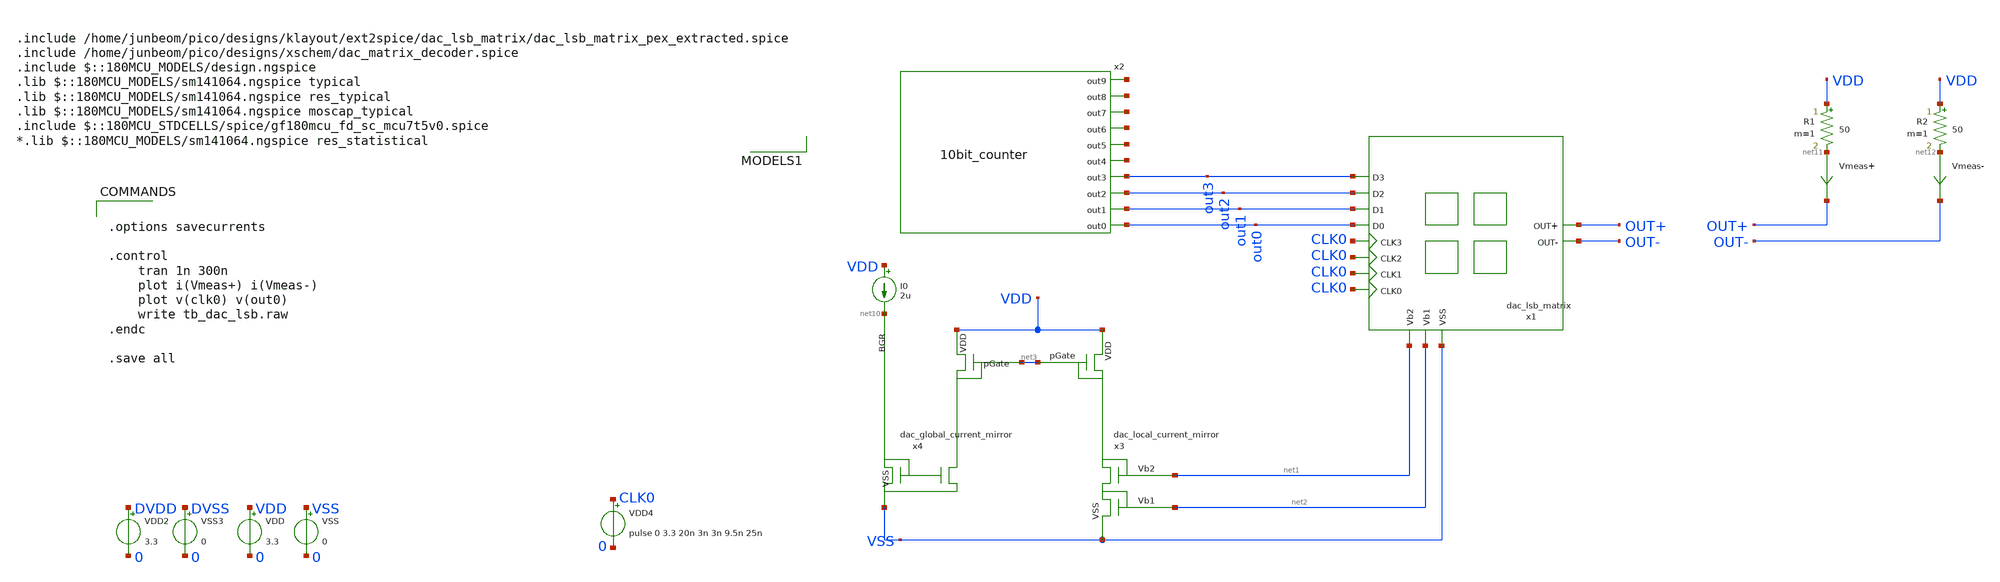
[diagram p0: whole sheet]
** sch_path: DAC/xschem/posim/tb/posim_tb_dac_lsb_matrix.sch
**.subckt posim_tb_dac_lsb_matrix
x2 out0 out1 out2 out3 net4 net5 net6 net7 net8 net9 10bit_counter
VDD VDD 0 3.3
VSS VSS 0 0
VDD2 DVDD 0 3.3
VSS3 DVSS 0 0
x3 VDD net3 net1 net2 VSS dac_local_current_mirror
x4 VDD net3 net10 VSS dac_global_current_mirror
I0 VDD net10 2u
R1 VDD net11 50 m=1
R2 VDD net12 50 m=1
Vmeas+ net11 OUT+ 0
.save i(vmeas+)
Vmeas- net12 OUT- 0
.save i(vmeas-)
x1 out3 out2 out1 out0 CLK0 CLK0 CLK0 CLK0 net1 net2 VSS OUT+ OUT- DVDD VSS dac_lsb_matrix
VDD4 CLK0 0 pulse 0 3.3 20n 3n 3n 9.5n 25n
**** begin user architecture code


.options savecurrents

.control
    tran 1n 300n
    plot i(Vmeas+) i(Vmeas-)
    plot v(clk0) v(out0)
    write tb_dac_lsb.raw
.endc

.save all



.include /home/junbeom/pico/designs/klayout/ext2spice/dac_lsb_matrix/dac_lsb_matrix_pex_extracted.spice
.include /home/junbeom/pico/designs/xschem/dac_matrix_decoder.spice
.include $::180MCU_MODELS/design.ngspice
.lib $::180MCU_MODELS/sm141064.ngspice typical
.lib $::180MCU_MODELS/sm141064.ngspice res_typical
.lib $::180MCU_MODELS/sm141064.ngspice moscap_typical
.include $::180MCU_STDCELLS/spice/gf180mcu_fd_sc_mcu7t5v0.spice
*.lib $::180MCU_MODELS/sm141064.ngspice res_statistical

**** end user architecture code
**.ends

* expanding   symbol:  10bit_counter.sym # of pins=10
** sym_path: DAC/xschem/10bit_counter.sym
.include /home/junbeom/pico/designs/xschem/10bit_Counter.sp

* expanding   symbol:  dac_local_current_mirror.sym # of pins=5
** sym_path: DAC/xschem/dac_local_current_mirror.sym
** sch_path: DAC/xschem/dac_local_current_mirror.sch
.subckt dac_local_current_mirror VDD pGate Vb2 Vb1 VSS
*.ipin VSS
*.opin Vb2
*.opin Vb1
*.ipin VDD
*.ipin pGate
XM2 Vb2 pGate VDD VDD pfet_03v3 L=1u W=5u nf=5 ad='int((nf+1)/2) * W/nf * 0.18u' as='int((nf+2)/2) * W/nf * 0.18u'
+ pd='2*int((nf+1)/2) * (W/nf + 0.18u)' ps='2*int((nf+2)/2) * (W/nf + 0.18u)' nrd='0.18u / W' nrs='0.18u / W'
+ sa=0 sb=0 sd=0 m=1
XM5 Vb2 Vb2 Vb1 VSS nfet_03v3 L=1u W=4u nf=4 ad='int((nf+1)/2) * W/nf * 0.18u' as='int((nf+2)/2) * W/nf * 0.18u'
+ pd='2*int((nf+1)/2) * (W/nf + 0.18u)' ps='2*int((nf+2)/2) * (W/nf + 0.18u)' nrd='0.18u / W' nrs='0.18u / W'
+ sa=0 sb=0 sd=0 m=1
XM6 Vb1 Vb1 VSS VSS nfet_03v3 L=1u W=4u nf=4 ad='int((nf+1)/2) * W/nf * 0.18u' as='int((nf+2)/2) * W/nf * 0.18u'
+ pd='2*int((nf+1)/2) * (W/nf + 0.18u)' ps='2*int((nf+2)/2) * (W/nf + 0.18u)' nrd='0.18u / W' nrs='0.18u / W'
+ sa=0 sb=0 sd=0 m=1
.ends


* expanding   symbol:  dac_global_current_mirror.sym # of pins=4
** sym_path: DAC/xschem/dac_global_current_mirror.sym
** sch_path: DAC/xschem/dac_global_current_mirror.sch
.subckt dac_global_current_mirror VDD pGate BGR VSS
*.ipin BGR
*.ipin VDD
*.opin pGate
*.ipin VSS
XM1 pGate pGate VDD VDD pfet_03v3 L=1u W=1u nf=1 ad='int((nf+1)/2) * W/nf * 0.18u' as='int((nf+2)/2) * W/nf * 0.18u'
+ pd='2*int((nf+1)/2) * (W/nf + 0.18u)' ps='2*int((nf+2)/2) * (W/nf + 0.18u)' nrd='0.18u / W' nrs='0.18u / W'
+ sa=0 sb=0 sd=0 m=1
XMN1 BGR BGR VSS VSS nfet_03v3 L=4u W=1u nf=4 ad='int((nf+1)/2) * W/nf * 0.18u' as='int((nf+2)/2) * W/nf * 0.18u'
+ pd='2*int((nf+1)/2) * (W/nf + 0.18u)' ps='2*int((nf+2)/2) * (W/nf + 0.18u)' nrd='0.18u / W' nrs='0.18u / W'
+ sa=0 sb=0 sd=0 m=1
XMN2 pGate BGR VSS VSS nfet_03v3 L=4u W=1u nf=4 ad='int((nf+1)/2) * W/nf * 0.18u' as='int((nf+2)/2) * W/nf * 0.18u'
+ pd='2*int((nf+1)/2) * (W/nf + 0.18u)' ps='2*int((nf+2)/2) * (W/nf + 0.18u)' nrd='0.18u / W' nrs='0.18u / W'
+ sa=0 sb=0 sd=0 m=1
.ends

.end
